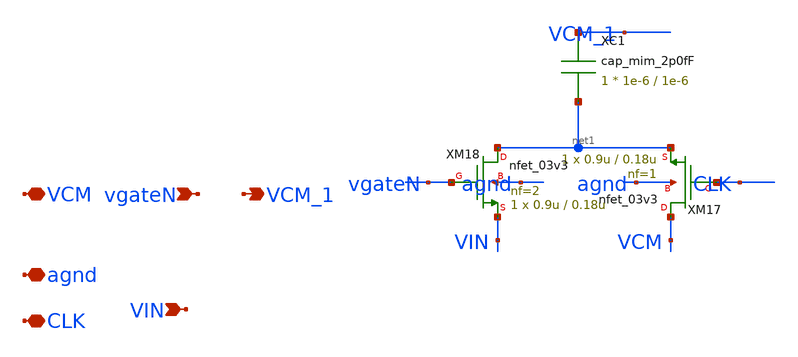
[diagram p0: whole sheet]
** sch_path: mpw18h1/cisar-gen/xschem/TBD/sample_unit_N.sch
**.subckt sample_unit_N VCM vgateN VCM_1 agnd VIN CLK
*.iopin VCM
*.ipin vgateN
*.opin VCM_1
*.iopin agnd
*.ipin VIN
*.iopin CLK
XM17 VCM CLK net1 agnd nfet_03v3 L=0.18u W=0.9u nf=1 ad='int((nf+1)/2) * W/nf * 0.18u' as='int((nf+2)/2) * W/nf * 0.18u'
+ pd='2*int((nf+1)/2) * (W/nf + 0.18u)' ps='2*int((nf+2)/2) * (W/nf + 0.18u)' nrd='0.18u / W' nrs='0.18u / W'
+ sa=0 sb=0 sd=0 m=1 par=1
XM18 net1 vgateN VIN agnd nfet_03v3 L=0.18u W=0.9u nf=2 ad='int((nf+1)/2) * W/nf * 0.18u' as='int((nf+2)/2) * W/nf * 0.18u'
+ pd='2*int((nf+1)/2) * (W/nf + 0.18u)' ps='2*int((nf+2)/2) * (W/nf + 0.18u)' nrd='0.18u / W' nrs='0.18u / W'
+ sa=0 sb=0 sd=0 m=1 par=1
XC1 VCM_1 net1 cap_mim_2p0fF c_width=1e-6 c_length=1e-6 m=1
**.ends
.end
